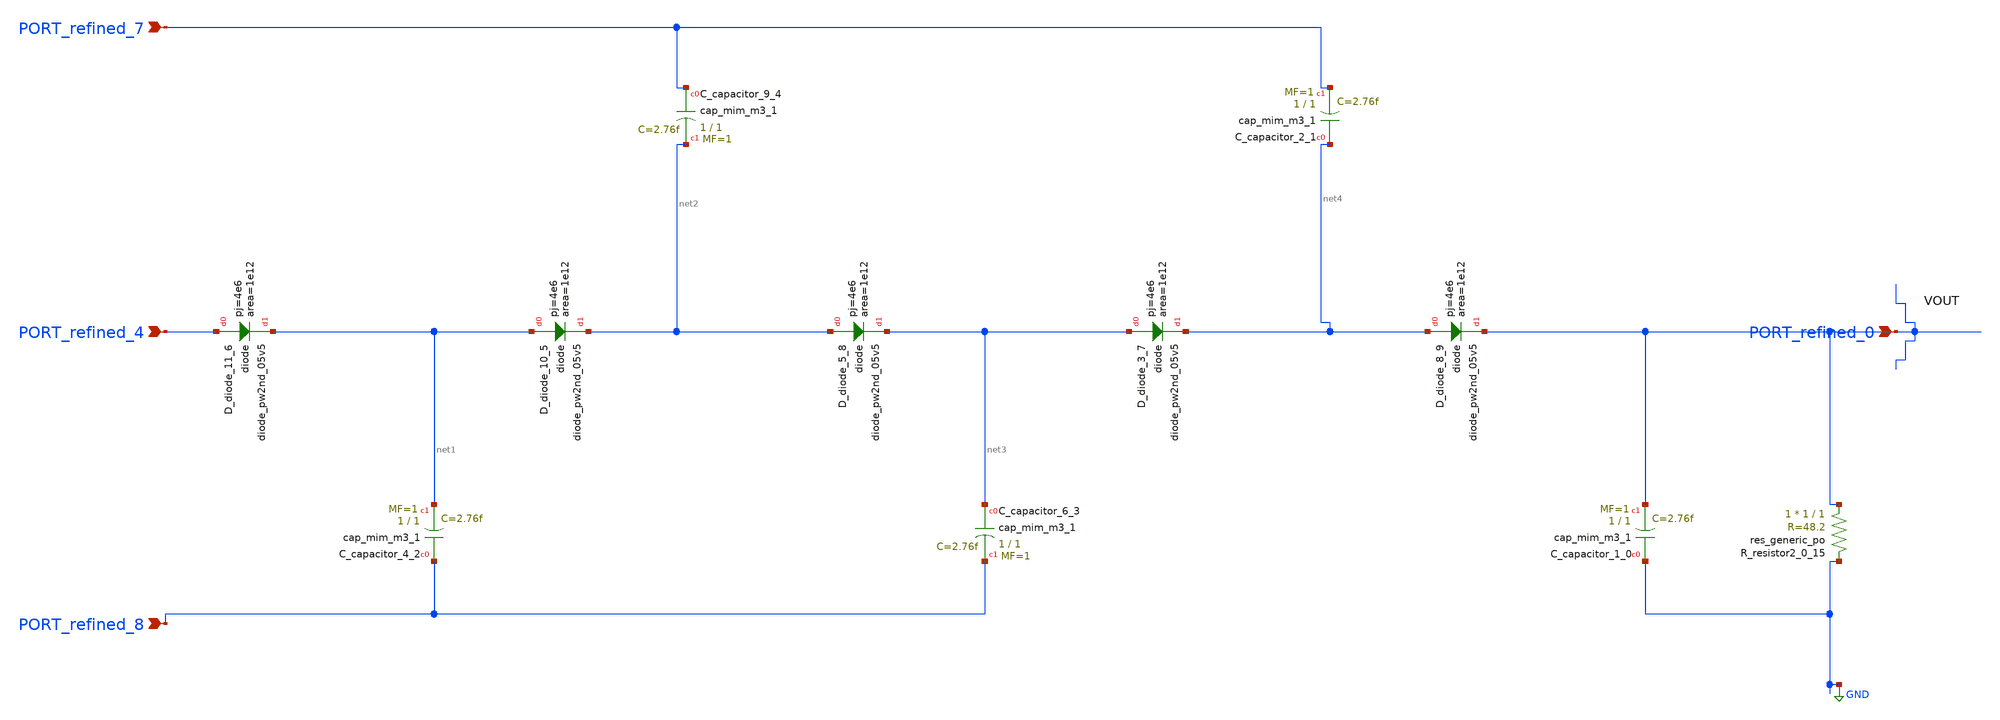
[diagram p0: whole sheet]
** sch_path: schematics/SchemGen/10_1109_ACCESS_2021_3050170_02_001.sch
**.subckt 10_1109_ACCESS_2021_3050170_02_001 PORT_refined_4 PORT_refined_8 PORT_refined_7
*+ PORT_refined_0
*.ipin PORT_refined_4
*.ipin PORT_refined_8
*.ipin PORT_refined_7
*.ipin PORT_refined_0
XC_capacitor_1_0 GND PORT_refined_0 sky130_fd_pr__cap_mim_m3_1 W=1 L=1 MF=1 m=1
XC_capacitor_2_1 net4 PORT_refined_7 sky130_fd_pr__cap_mim_m3_1 W=1 L=1 MF=1 m=1
XC_capacitor_4_2 PORT_refined_8 net1 sky130_fd_pr__cap_mim_m3_1 W=1 L=1 MF=1 m=1
XC_capacitor_6_3 net3 PORT_refined_8 sky130_fd_pr__cap_mim_m3_1 W=1 L=1 MF=1 m=1
XC_capacitor_9_4 PORT_refined_7 net2 sky130_fd_pr__cap_mim_m3_1 W=1 L=1 MF=1 m=1
XD_diode_10_5 net1 net2 sky130_fd_pr__diode_pw2nd_05v5 area=1e12 pj=4e6
XD_diode_11_6 PORT_refined_4 net1 sky130_fd_pr__diode_pw2nd_05v5 area=1e12 pj=4e6
XD_diode_3_7 net3 net4 sky130_fd_pr__diode_pw2nd_05v5 area=1e12 pj=4e6
XD_diode_5_8 net2 net3 sky130_fd_pr__diode_pw2nd_05v5 area=1e12 pj=4e6
XD_diode_8_9 net4 PORT_refined_0 sky130_fd_pr__diode_pw2nd_05v5 area=1e12 pj=4e6
XR_resistor2_0_15 PORT_refined_0 GND sky130_fd_pr__res_generic_po W=1 L=1 m=1
**.ends
.GLOBAL GND
.end
